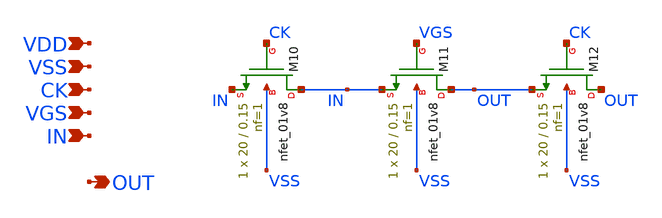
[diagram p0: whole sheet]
** sch_path: xschem/th_sw_main.sch
**.subckt th_sw_main VDD VSS CK VGS IN OUT
*.ipin VDD
*.ipin VSS
*.ipin CK
*.ipin VGS
*.ipin IN
*.opin OUT
XM10 IN CK IN VSS sky130_fd_pr__nfet_01v8 L=0.15 W=20 nf=1 ad='int((nf+1)/2) * W/nf * 0.29' as='int((nf+2)/2) * W/nf * 0.29'
+ pd='2*int((nf+1)/2) * (W/nf + 0.29)' ps='2*int((nf+2)/2) * (W/nf + 0.29)' nrd='0.29 / W' nrs='0.29 / W'
+ sa=0 sb=0 sd=0 mult=1 m=1
XM11 OUT VGS IN VSS sky130_fd_pr__nfet_01v8 L=0.15 W=20 nf=1 ad='int((nf+1)/2) * W/nf * 0.29' as='int((nf+2)/2) * W/nf * 0.29'
+ pd='2*int((nf+1)/2) * (W/nf + 0.29)' ps='2*int((nf+2)/2) * (W/nf + 0.29)' nrd='0.29 / W' nrs='0.29 / W'
+ sa=0 sb=0 sd=0 mult=1 m=1
XM12 OUT CK OUT VSS sky130_fd_pr__nfet_01v8 L=0.15 W=20 nf=1 ad='int((nf+1)/2) * W/nf * 0.29' as='int((nf+2)/2) * W/nf * 0.29'
+ pd='2*int((nf+1)/2) * (W/nf + 0.29)' ps='2*int((nf+2)/2) * (W/nf + 0.29)' nrd='0.29 / W' nrs='0.29 / W'
+ sa=0 sb=0 sd=0 mult=1 m=1
**.ends
.end
